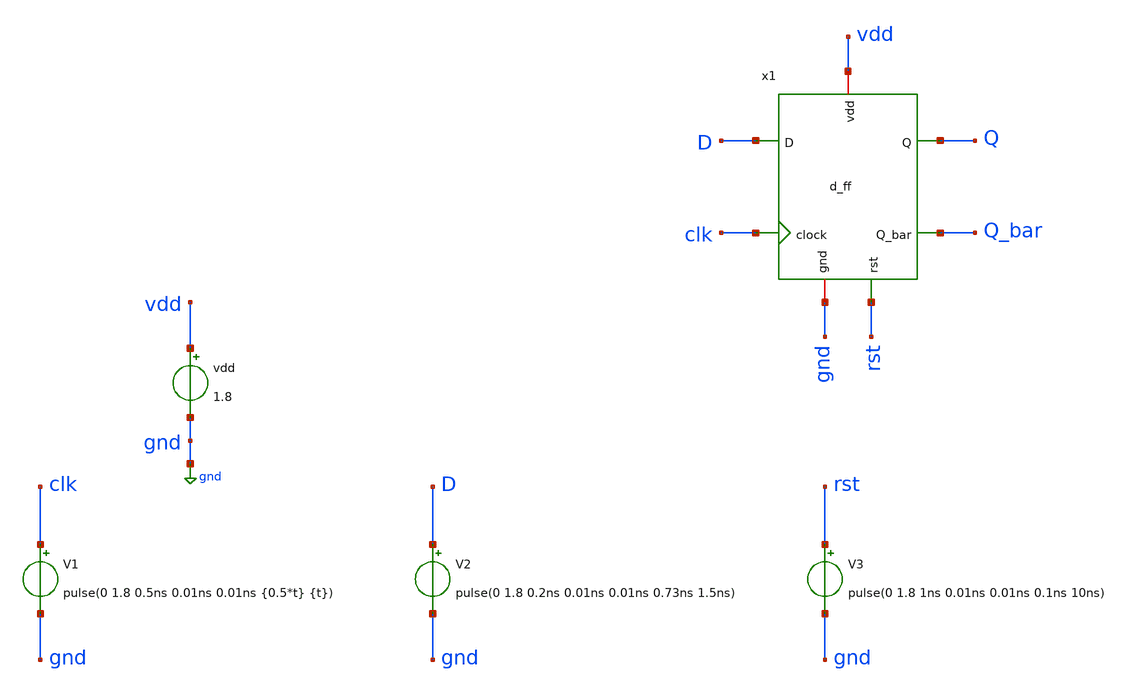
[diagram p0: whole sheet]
** sch_path: SequentialCircuits/D_ff/d_ff_tb.sch
**.subckt d_ff_tb
vdd vdd gnd 1.8
V1 clk gnd pulse(0 1.8 0.5ns 0.01ns 0.01ns {0.5*t} {t})
V2 D gnd pulse(0 1.8 0.2ns 0.01ns 0.01ns 0.73ns 1.5ns)
x1 vdd D Q clk Q_bar rst gnd d_ff
V3 rst gnd pulse(0 1.8 1ns 0.01ns 0.01ns 0.1ns 10ns)
**** begin user architecture code


.lib /usr/local/share/pdk/sky130A/libs.tech/ngspice/sky130.lib.spice tt

.param fs=0.5e09 t=1/fs w_reset_mos=2.5

.control
    tran 0.1n 20n
    plot clk D
    plot clk Q
    plot Q Q_bar
.endc

.save all

**** end user architecture code
**.ends

* expanding   symbol:  SequentialCircuits/D_ff/d_ff.sym # of pins=7
** sym_path: SequentialCircuits/D_ff/d_ff.sym
** sch_path: SequentialCircuits/D_ff/d_ff.sch
.subckt d_ff vdd D Q clock Q_bar rst gnd
*.ipin D
*.ipin clock
*.ipin rst
*.iopin vdd
*.iopin gnd
*.opin Q
*.opin Q_bar
x2 vdd gnd net4 net2 not
x3 vdd gnd D net3 not
XM1 net2 clkc net1 vdd sky130_fd_pr__pfet_01v8 L=0.15 W=1 nf=1 ad='int((nf+1)/2) * W/nf * 0.29' as='int((nf+2)/2) * W/nf * 0.29'
+ pd='2*int((nf+1)/2) * (W/nf + 0.29)' ps='2*int((nf+2)/2) * (W/nf + 0.29)' nrd='0.29 / W' nrs='0.29 / W'
+ sa=0 sb=0 sd=0 mult=1 m=1
XM2 net3 clk net1 vdd sky130_fd_pr__pfet_01v8 L=0.15 W=1 nf=1 ad='int((nf+1)/2) * W/nf * 0.29' as='int((nf+2)/2) * W/nf * 0.29'
+ pd='2*int((nf+1)/2) * (W/nf + 0.29)' ps='2*int((nf+2)/2) * (W/nf + 0.29)' nrd='0.29 / W' nrs='0.29 / W'
+ sa=0 sb=0 sd=0 mult=1 m=1
XM3 net2 clk net1 gnd sky130_fd_pr__nfet_01v8 L=0.15 W=1 nf=1 ad='int((nf+1)/2) * W/nf * 0.29' as='int((nf+2)/2) * W/nf * 0.29'
+ pd='2*int((nf+1)/2) * (W/nf + 0.29)' ps='2*int((nf+2)/2) * (W/nf + 0.29)' nrd='0.29 / W' nrs='0.29 / W'
+ sa=0 sb=0 sd=0 mult=1 m=1
XM4 net3 clkc net1 gnd sky130_fd_pr__nfet_01v8 L=0.15 W=1 nf=1 ad='int((nf+1)/2) * W/nf * 0.29' as='int((nf+2)/2) * W/nf * 0.29'
+ pd='2*int((nf+1)/2) * (W/nf + 0.29)' ps='2*int((nf+2)/2) * (W/nf + 0.29)' nrd='0.29 / W' nrs='0.29 / W'
+ sa=0 sb=0 sd=0 mult=1 m=1
x4 vdd gnd net1 net4 not
x5 vdd gnd Q net6 not
x6 vdd gnd net4 net7 not
XM5 net6 clk net5 vdd sky130_fd_pr__pfet_01v8 L=0.15 W=1 nf=1 ad='int((nf+1)/2) * W/nf * 0.29' as='int((nf+2)/2) * W/nf * 0.29'
+ pd='2*int((nf+1)/2) * (W/nf + 0.29)' ps='2*int((nf+2)/2) * (W/nf + 0.29)' nrd='0.29 / W' nrs='0.29 / W'
+ sa=0 sb=0 sd=0 mult=1 m=1
XM6 net7 clkc net5 vdd sky130_fd_pr__pfet_01v8 L=0.3 W=1 nf=1 ad='int((nf+1)/2) * W/nf * 0.29' as='int((nf+2)/2) * W/nf * 0.29'
+ pd='2*int((nf+1)/2) * (W/nf + 0.29)' ps='2*int((nf+2)/2) * (W/nf + 0.29)' nrd='0.29 / W' nrs='0.29 / W'
+ sa=0 sb=0 sd=0 mult=1 m=1
XM7 net6 clkc net5 gnd sky130_fd_pr__nfet_01v8 L=0.15 W=1 nf=1 ad='int((nf+1)/2) * W/nf * 0.29' as='int((nf+2)/2) * W/nf * 0.29'
+ pd='2*int((nf+1)/2) * (W/nf + 0.29)' ps='2*int((nf+2)/2) * (W/nf + 0.29)' nrd='0.29 / W' nrs='0.29 / W'
+ sa=0 sb=0 sd=0 mult=1 m=1
XM8 net7 clk net5 gnd sky130_fd_pr__nfet_01v8 L=0.3 W=1 nf=1 ad='int((nf+1)/2) * W/nf * 0.29' as='int((nf+2)/2) * W/nf * 0.29'
+ pd='2*int((nf+1)/2) * (W/nf + 0.29)' ps='2*int((nf+2)/2) * (W/nf + 0.29)' nrd='0.29 / W' nrs='0.29 / W'
+ sa=0 sb=0 sd=0 mult=1 m=1
x7 vdd gnd net5 Q not
XM9 Q rst gnd gnd sky130_fd_pr__nfet_01v8 L=0.15 W=w_reset_mos nf=1 ad='int((nf+1)/2) * W/nf * 0.29'
+ as='int((nf+2)/2) * W/nf * 0.29' pd='2*int((nf+1)/2) * (W/nf + 0.29)' ps='2*int((nf+2)/2) * (W/nf + 0.29)'
+ nrd='0.29 / W' nrs='0.29 / W' sa=0 sb=0 sd=0 mult=1 m=1
x1 vdd clk clock clkc gnd non_overlapping_clk_gen
XM10 Q_bar Q gnd gnd sky130_fd_pr__nfet_01v8 L=0.15 W=1 nf=1 ad='int((nf+1)/2) * W/nf * 0.29' as='int((nf+2)/2) * W/nf * 0.29'
+ pd='2*int((nf+1)/2) * (W/nf + 0.29)' ps='2*int((nf+2)/2) * (W/nf + 0.29)' nrd='0.29 / W' nrs='0.29 / W'
+ sa=0 sb=0 sd=0 mult=1 m=1
XM11 Q_bar Q vdd vdd sky130_fd_pr__pfet_01v8 L=0.15 W=3 nf=1 ad='int((nf+1)/2) * W/nf * 0.29' as='int((nf+2)/2) * W/nf * 0.29'
+ pd='2*int((nf+1)/2) * (W/nf + 0.29)' ps='2*int((nf+2)/2) * (W/nf + 0.29)' nrd='0.29 / W' nrs='0.29 / W'
+ sa=0 sb=0 sd=0 mult=1 m=1
.ends


* expanding   symbol:  LogicGates/not.sym # of pins=4
** sym_path: LogicGates/not.sym
** sch_path: LogicGates/not.sch
.subckt not vdd gnd vin vout
*.ipin vin
*.iopin vdd
*.iopin gnd
*.opin vout
XM2 vout vin vdd vdd sky130_fd_pr__pfet_01v8 L=0.15 W=2 nf=1 ad='int((nf+1)/2) * W/nf * 0.29' as='int((nf+2)/2) * W/nf * 0.29'
+ pd='2*int((nf+1)/2) * (W/nf + 0.29)' ps='2*int((nf+2)/2) * (W/nf + 0.29)' nrd='0.29 / W' nrs='0.29 / W'
+ sa=0 sb=0 sd=0 mult=1 m=1
XM1 vout vin gnd gnd sky130_fd_pr__nfet_01v8 L=0.15 W=1 nf=1 ad='int((nf+1)/2) * W/nf * 0.29' as='int((nf+2)/2) * W/nf * 0.29'
+ pd='2*int((nf+1)/2) * (W/nf + 0.29)' ps='2*int((nf+2)/2) * (W/nf + 0.29)' nrd='0.29 / W' nrs='0.29 / W'
+ sa=0 sb=0 sd=0 mult=1 m=1
.ends


* expanding   symbol:  SequentialCircuits/Non Overlapping Clock
*+ Generator/non_overlapping_clk_gen.sym # of pins=5
** sym_path: SequentialCircuits/Non Overlapping Clock Generator/non_overlapping_clk_gen.sym
** sch_path: SequentialCircuits/Non Overlapping Clock Generator/non_overlapping_clk_gen.sch
.subckt non_overlapping_clk_gen vdd phi1 clk phi2 gnd
*.ipin clk
*.iopin vdd
*.iopin gnd
*.opin phi1
*.opin phi2
x1 vdd gnd clk net1 not
x2 vdd gnd net1 phi2 phi1 nor
x3 vdd gnd phi1 clk phi2 nor
.ends


* expanding   symbol:  LogicGates/nor.sym # of pins=5
** sym_path: LogicGates/nor.sym
** sch_path: LogicGates/nor.sch
.subckt nor vdd gnd A B Y
*.ipin A
*.ipin B
*.iopin vdd
*.iopin gnd
*.opin Y
XM1 Y A gnd gnd sky130_fd_pr__nfet_01v8 L=0.15 W=1 nf=1 ad='int((nf+1)/2) * W/nf * 0.29' as='int((nf+2)/2) * W/nf * 0.29'
+ pd='2*int((nf+1)/2) * (W/nf + 0.29)' ps='2*int((nf+2)/2) * (W/nf + 0.29)' nrd='0.29 / W' nrs='0.29 / W'
+ sa=0 sb=0 sd=0 mult=1 m=1
XM2 Y B gnd gnd sky130_fd_pr__nfet_01v8 L=0.15 W=1 nf=1 ad='int((nf+1)/2) * W/nf * 0.29' as='int((nf+2)/2) * W/nf * 0.29'
+ pd='2*int((nf+1)/2) * (W/nf + 0.29)' ps='2*int((nf+2)/2) * (W/nf + 0.29)' nrd='0.29 / W' nrs='0.29 / W'
+ sa=0 sb=0 sd=0 mult=1 m=1
XM3 net1 A vdd vdd sky130_fd_pr__pfet_01v8 L=0.15 W=2 nf=1 ad='int((nf+1)/2) * W/nf * 0.29' as='int((nf+2)/2) * W/nf * 0.29'
+ pd='2*int((nf+1)/2) * (W/nf + 0.29)' ps='2*int((nf+2)/2) * (W/nf + 0.29)' nrd='0.29 / W' nrs='0.29 / W'
+ sa=0 sb=0 sd=0 mult=1 m=1
XM4 Y B net1 vdd sky130_fd_pr__pfet_01v8 L=0.15 W=2 nf=1 ad='int((nf+1)/2) * W/nf * 0.29' as='int((nf+2)/2) * W/nf * 0.29'
+ pd='2*int((nf+1)/2) * (W/nf + 0.29)' ps='2*int((nf+2)/2) * (W/nf + 0.29)' nrd='0.29 / W' nrs='0.29 / W'
+ sa=0 sb=0 sd=0 mult=1 m=1
.ends

.GLOBAL gnd
.end
